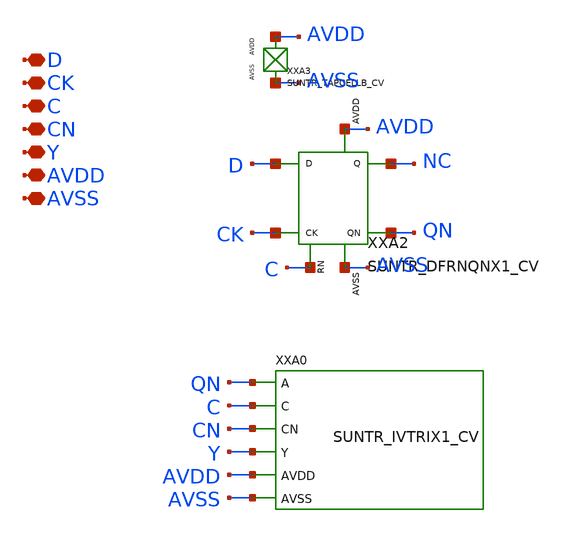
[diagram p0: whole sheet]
** sch_path: design/SUN_TR_SKY130NM/SUNTR_DFTRIX1_CV.sch
**.subckt SUNTR_DFTRIX1_CV D CK C CN Y AVDD AVSS
*.iopin D
*.iopin CK
*.iopin C
*.iopin CN
*.iopin Y
*.iopin AVDD
*.iopin AVSS
XXA3 AVDD AVSS SUNTR_TAPCELLB_CV xoffset=0 yoffset=0 angle=0
XXA2 D CK C NC QN AVDD AVSS SUNTR_DFRNQNX1_CV xoffset=0 yoffset=0 angle=0
XXA0 QN C CN Y AVDD AVSS SUNTR_IVTRIX1_CV xoffset=0 yoffset=0 angle=0
**.ends
.end
